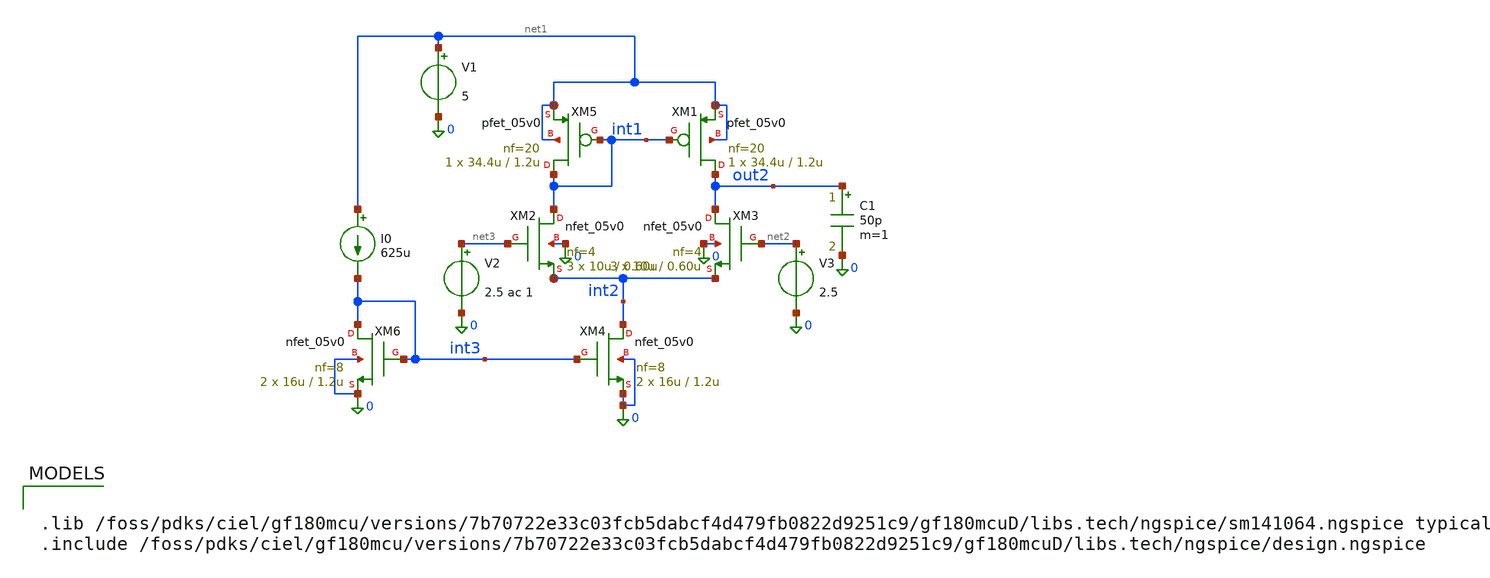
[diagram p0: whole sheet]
** sch_path: RN_Gm3/gm3_ota_tb (1).sch
**.subckt gm3_ota_tb (1)
V1 net1 0 5
V2 net3 0 2.5 ac 1
V3 net2 0 2.5
C1 out2 0 50p m=1
I0 net1 int3 625u
XM6 int3 int3 0 0 nfet_05v0 L=1.2u W=16u nf=8 ad='int((nf+1)/2) * W/nf * 0.18u' as='int((nf+2)/2) * W/nf * 0.18u'
+ pd='2*int((nf+1)/2) * (W/nf + 0.18u)' ps='2*int((nf+2)/2) * (W/nf + 0.18u)' nrd='0.18u / W' nrs='0.18u / W'
+ sa=0 sb=0 sd=0 m=2
XM5 int1 int1 net1 net1 pfet_05v0 L=1.2u W=34.4u nf=20 ad='int((nf+1)/2) * W/nf * 0.18u' as='int((nf+2)/2) * W/nf * 0.18u'
+ pd='2*int((nf+1)/2) * (W/nf + 0.18u)' ps='2*int((nf+2)/2) * (W/nf + 0.18u)' nrd='0.18u / W' nrs='0.18u / W'
+ sa=0 sb=0 sd=0 m=1
XM1 out2 int1 net1 net1 pfet_05v0 L=1.2u W=34.4u nf=20 ad='int((nf+1)/2) * W/nf * 0.18u' as='int((nf+2)/2) * W/nf * 0.18u'
+ pd='2*int((nf+1)/2) * (W/nf + 0.18u)' ps='2*int((nf+2)/2) * (W/nf + 0.18u)' nrd='0.18u / W' nrs='0.18u / W'
+ sa=0 sb=0 sd=0 m=1
XM2 int1 net3 int2 0 nfet_05v0 L=0.60u W=10u nf=4 ad='int((nf+1)/2) * W/nf * 0.18u' as='int((nf+2)/2) * W/nf * 0.18u'
+ pd='2*int((nf+1)/2) * (W/nf + 0.18u)' ps='2*int((nf+2)/2) * (W/nf + 0.18u)' nrd='0.18u / W' nrs='0.18u / W'
+ sa=0 sb=0 sd=0 m=3
XM3 out2 net2 int2 0 nfet_05v0 L=0.60u W=10u nf=4 ad='int((nf+1)/2) * W/nf * 0.18u' as='int((nf+2)/2) * W/nf * 0.18u'
+ pd='2*int((nf+1)/2) * (W/nf + 0.18u)' ps='2*int((nf+2)/2) * (W/nf + 0.18u)' nrd='0.18u / W' nrs='0.18u / W'
+ sa=0 sb=0 sd=0 m=3
XM4 int2 int3 0 0 nfet_05v0 L=1.2u W=16u nf=8 ad='int((nf+1)/2) * W/nf * 0.18u' as='int((nf+2)/2) * W/nf * 0.18u'
+ pd='2*int((nf+1)/2) * (W/nf + 0.18u)' ps='2*int((nf+2)/2) * (W/nf + 0.18u)' nrd='0.18u / W' nrs='0.18u / W'
+ sa=0 sb=0 sd=0 m=2
**** begin user architecture code


.lib /foss/pdks/ciel/gf180mcu/versions/7b70722e33c03fcb5dabcf4d479fb0822d9251c9/gf180mcuD/libs.tech/ngspice/sm141064.ngspice typical
.include /foss/pdks/ciel/gf180mcu/versions/7b70722e33c03fcb5dabcf4d479fb0822d9251c9/gf180mcuD/libs.tech/ngspice/design.ngspice




.control
  	save all
	op
	ac dec 20 1 100Meg
	remzerovec
	write gm3_OTA_ac.raw
.endc

.options savecurrents


**** end user architecture code
**.ends
.end
